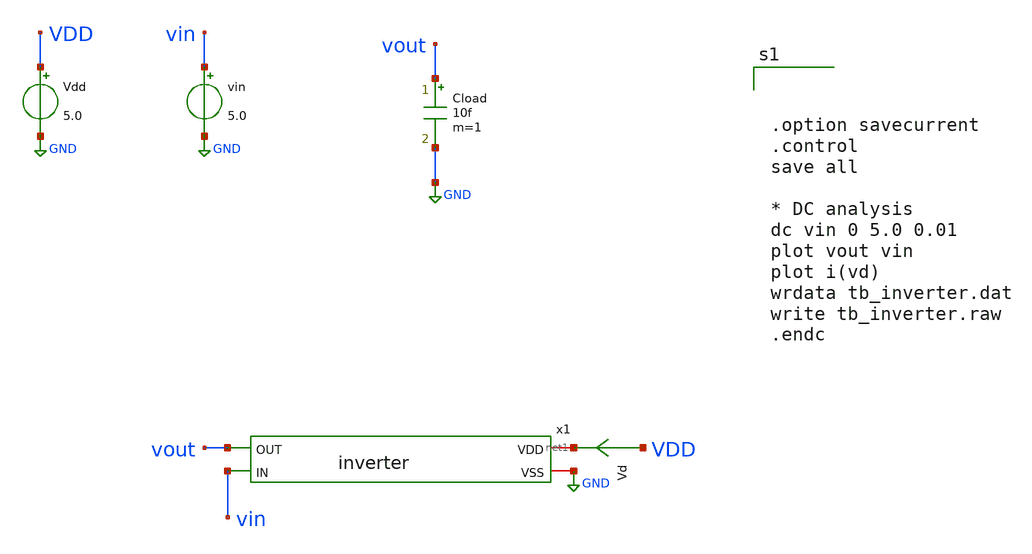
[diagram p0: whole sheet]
** sch_path: member_project/inverter/RISE-A/7158918/tb_inverter.sch
**.subckt tb_inverter
Vdd VDD GND 5.0
Vd VDD net1 0
.save i(vd)
vin vin GND 5.0
x1 net1 vout vin GND inverter
Cload vout GND 10f m=1
**** begin user architecture code



.option savecurrent
.control
save all

* DC analysis
dc vin 0 5.0 0.01
plot vout vin
plot i(vd)
wrdata tb_inverter.dat
write tb_inverter.raw
.endc




 .include $::LIB/ip62_models
**** end user architecture code
**.ends

* expanding   symbol:  inverter.sym # of pins=4
** sym_path: member_project/inverter/RISE-A/7158918/inverter.sym
** sch_path: member_project/inverter/RISE-A/7158918/inverter.sch
.subckt inverter VDD OUT IN VSS
*.ipin OUT
*.ipin IN
*.iopin VDD
*.iopin VSS
XXM1 OUT IN VDD VDD PMOS w=3.4u l=1u nrd=0 nrs=0 m=1
XXM2 OUT IN VSS VSS NMOS w=3.4u l=1u nrd=0 nrs=0 m=1
.ends

.GLOBAL GND
.end
